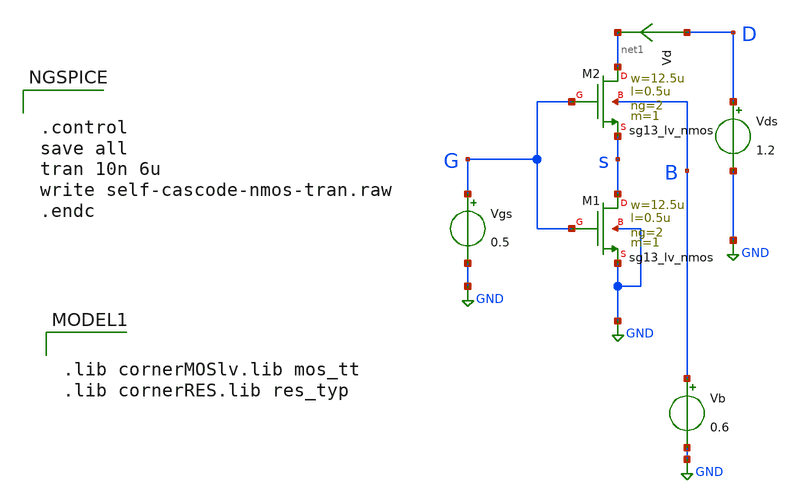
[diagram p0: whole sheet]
** sch_path: xschem/self-cascode-nmos-tran.sch
**.subckt self-cascode-nmos-tran
Vgs G GND 0.5
Vds D GND 1.2
Vd D net1 0
.save i(vd)
XM1 s G GND GND sg13_lv_nmos w=12.5u l=0.5u ng=2 m=1 mm_ok=1
XM2 net1 G s B sg13_lv_nmos w=12.5u l=0.5u ng=2 m=1 mm_ok=1
Vb B GND 0.6
**** begin user architecture code


.control
save all
tran 10n 6u
write self-cascode-nmos-tran.raw
.endc



.lib cornerMOSlv.lib mos_tt
.lib cornerRES.lib res_typ

**** end user architecture code
**.ends
.GLOBAL GND
.end
